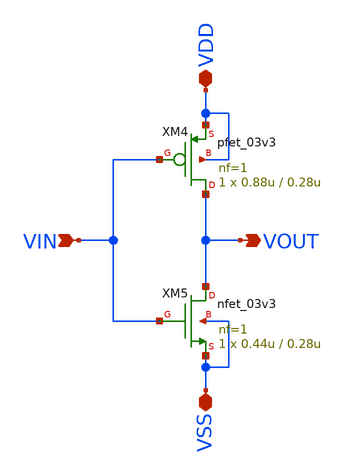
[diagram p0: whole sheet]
** sch_path: Clock_Generator_PAKISTAN_06/Schematics/untitled-6.sch
**.subckt untitled-6 VDD VIN VOUT VSS
*.iopin VDD
*.ipin VIN
*.opin VOUT
*.iopin VSS
XM4 VOUT VIN VDD VDD pfet_03v3 L=0.28u W=0.88u nf=1 ad='int((nf+1)/2) * W/nf * 0.18u' as='int((nf+2)/2) * W/nf * 0.18u'
+ pd='2*int((nf+1)/2) * (W/nf + 0.18u)' ps='2*int((nf+2)/2) * (W/nf + 0.18u)' nrd='0.18u / W' nrs='0.18u / W'
+ sa=0 sb=0 sd=0 m=1
XM5 VOUT VIN VSS VSS nfet_03v3 L=0.28u W=0.44u nf=1 ad='int((nf+1)/2) * W/nf * 0.18u' as='int((nf+2)/2) * W/nf * 0.18u'
+ pd='2*int((nf+1)/2) * (W/nf + 0.18u)' ps='2*int((nf+2)/2) * (W/nf + 0.18u)' nrd='0.18u / W' nrs='0.18u / W'
+ sa=0 sb=0 sd=0 m=1
**.ends
.end
